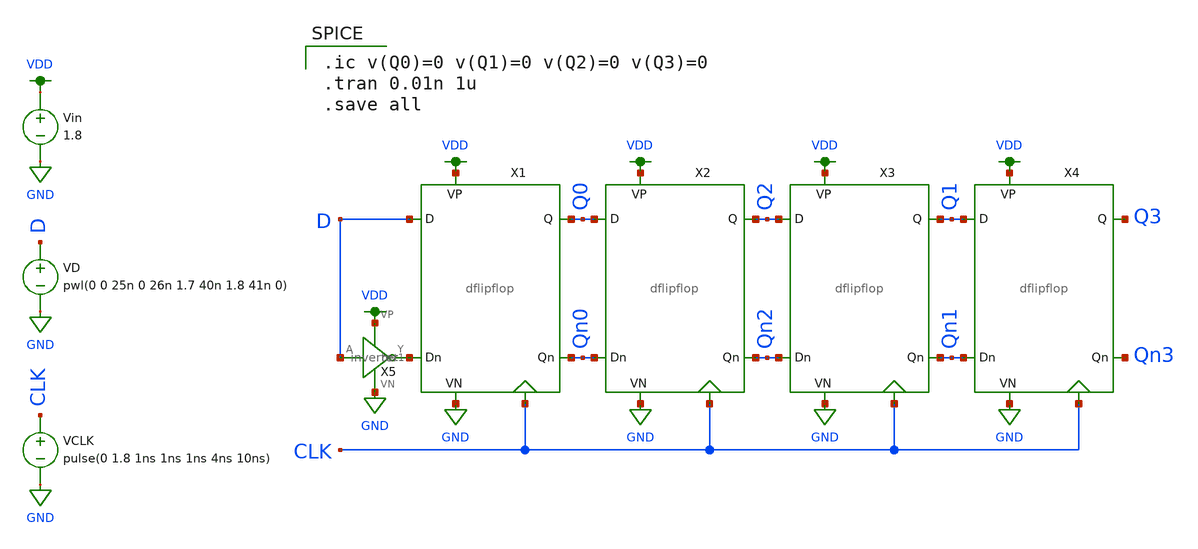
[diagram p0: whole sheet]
** sch_path: miniproject_02/xschem/shiftreg4_tran.sch
**.subckt shiftreg4_tran
X1 D Q0 VDD GND net1 Qn0 CLK dflipflop
X2 Q0 Q2 VDD GND Qn0 Qn2 CLK dflipflop
X3 Q2 Q1 VDD GND Qn2 Qn1 CLK dflipflop
X4 Q1 Q3 VDD GND Qn1 Qn3 CLK dflipflop
X5 D net1 VDD GND inverter
Vin VDD GND 1.8
VD D GND pwl(0 0 25n 0 26n 1.7 40n 1.8 41n 0)
VCLK CLK GND pulse(0 1.8 1ns 1ns 1ns 4ns 10ns)
**** begin user architecture code

.option wnflag=1
.lib ~/skywater/skywater-pdk/libraries/sky130_fd_pr_ngspice/latest/models/sky130.lib.spice tt


.ic v(Q0)=0 v(Q1)=0 v(Q2)=0 v(Q3)=0
.tran 0.01n 1u
.save all

**** end user architecture code
**.ends

* expanding   symbol:  ENGR3426-MADVLSI/miniproject_02/xschem/dflipflop.sym # of pins=7
** sym_path: miniproject_02/xschem/dflipflop.sym
** sch_path: miniproject_02/xschem/dflipflop.sch
.subckt dflipflop D Q VP VN Dn Qn CLK
*.ipin Dn
*.ipin D
*.opin Q
*.opin Qn
*.iopin CLK
*.iopin VP
*.iopin VN
XM1 net1 CLK D VDD sky130_fd_pr__pfet_01v8 L=0.15 W=1 nf=1 ad='int((nf+1)/2) * W/nf * 0.29' as='int((nf+2)/2) * W/nf * 0.29'
+ pd='2*int((nf+1)/2) * (W/nf + 0.29)' ps='2*int((nf+2)/2) * (W/nf + 0.29)' nrd='0.29 / W' nrs='0.29 / W'
+ sa=0 sb=0 sd=0 mult=1 m=1
XM2 net2 CLK Dn VDD sky130_fd_pr__pfet_01v8 L=0.15 W=1 nf=1 ad='int((nf+1)/2) * W/nf * 0.29' as='int((nf+2)/2) * W/nf * 0.29'
+ pd='2*int((nf+1)/2) * (W/nf + 0.29)' ps='2*int((nf+2)/2) * (W/nf + 0.29)' nrd='0.29 / W' nrs='0.29 / W'
+ sa=0 sb=0 sd=0 mult=1 m=1
XM3 Q CLK net1 GND sky130_fd_pr__nfet_01v8 L=0.15 W=1 nf=1 ad='int((nf+1)/2) * W/nf * 0.29' as='int((nf+2)/2) * W/nf * 0.29'
+ pd='2*int((nf+1)/2) * (W/nf + 0.29)' ps='2*int((nf+2)/2) * (W/nf + 0.29)' nrd='0.29 / W' nrs='0.29 / W'
+ sa=0 sb=0 sd=0 mult=1 m=1
XM4 Qn CLK net2 GND sky130_fd_pr__nfet_01v8 L=0.15 W=1 nf=1 ad='int((nf+1)/2) * W/nf * 0.29' as='int((nf+2)/2) * W/nf * 0.29'
+ pd='2*int((nf+1)/2) * (W/nf + 0.29)' ps='2*int((nf+2)/2) * (W/nf + 0.29)' nrd='0.29 / W' nrs='0.29 / W'
+ sa=0 sb=0 sd=0 mult=1 m=1
XM5 net4 CLK VN GND sky130_fd_pr__nfet_01v8 L=0.15 W=4 nf=1 ad='int((nf+1)/2) * W/nf * 0.29' as='int((nf+2)/2) * W/nf * 0.29'
+ pd='2*int((nf+1)/2) * (W/nf + 0.29)' ps='2*int((nf+2)/2) * (W/nf + 0.29)' nrd='0.29 / W' nrs='0.29 / W'
+ sa=0 sb=0 sd=0 mult=1 m=1
XM6 net2 net1 net4 GND sky130_fd_pr__nfet_01v8 L=0.15 W=1 nf=1 ad='int((nf+1)/2) * W/nf * 0.29' as='int((nf+2)/2) * W/nf * 0.29'
+ pd='2*int((nf+1)/2) * (W/nf + 0.29)' ps='2*int((nf+2)/2) * (W/nf + 0.29)' nrd='0.29 / W' nrs='0.29 / W'
+ sa=0 sb=0 sd=0 mult=1 m=1
XM7 net4 net2 net1 GND sky130_fd_pr__nfet_01v8 L=0.15 W=1 nf=1 ad='int((nf+1)/2) * W/nf * 0.29' as='int((nf+2)/2) * W/nf * 0.29'
+ pd='2*int((nf+1)/2) * (W/nf + 0.29)' ps='2*int((nf+2)/2) * (W/nf + 0.29)' nrd='0.29 / W' nrs='0.29 / W'
+ sa=0 sb=0 sd=0 mult=1 m=1
XM8 net2 net1 VP VDD sky130_fd_pr__pfet_01v8 L=0.15 W=1 nf=1 ad='int((nf+1)/2) * W/nf * 0.29' as='int((nf+2)/2) * W/nf * 0.29'
+ pd='2*int((nf+1)/2) * (W/nf + 0.29)' ps='2*int((nf+2)/2) * (W/nf + 0.29)' nrd='0.29 / W' nrs='0.29 / W'
+ sa=0 sb=0 sd=0 mult=1 m=1
XM9 VP net2 net1 VDD sky130_fd_pr__pfet_01v8 L=0.15 W=1 nf=1 ad='int((nf+1)/2) * W/nf * 0.29' as='int((nf+2)/2) * W/nf * 0.29'
+ pd='2*int((nf+1)/2) * (W/nf + 0.29)' ps='2*int((nf+2)/2) * (W/nf + 0.29)' nrd='0.29 / W' nrs='0.29 / W'
+ sa=0 sb=0 sd=0 mult=1 m=1
XM10 net3 CLK VP VDD sky130_fd_pr__pfet_01v8 L=0.15 W=4 nf=1 ad='int((nf+1)/2) * W/nf * 0.29' as='int((nf+2)/2) * W/nf * 0.29'
+ pd='2*int((nf+1)/2) * (W/nf + 0.29)' ps='2*int((nf+2)/2) * (W/nf + 0.29)' nrd='0.29 / W' nrs='0.29 / W'
+ sa=0 sb=0 sd=0 mult=1 m=1
XM11 Qn Q net3 VDD sky130_fd_pr__pfet_01v8 L=0.15 W=1 nf=1 ad='int((nf+1)/2) * W/nf * 0.29' as='int((nf+2)/2) * W/nf * 0.29'
+ pd='2*int((nf+1)/2) * (W/nf + 0.29)' ps='2*int((nf+2)/2) * (W/nf + 0.29)' nrd='0.29 / W' nrs='0.29 / W'
+ sa=0 sb=0 sd=0 mult=1 m=1
XM12 net3 Qn Q VDD sky130_fd_pr__pfet_01v8 L=0.15 W=1 nf=1 ad='int((nf+1)/2) * W/nf * 0.29' as='int((nf+2)/2) * W/nf * 0.29'
+ pd='2*int((nf+1)/2) * (W/nf + 0.29)' ps='2*int((nf+2)/2) * (W/nf + 0.29)' nrd='0.29 / W' nrs='0.29 / W'
+ sa=0 sb=0 sd=0 mult=1 m=1
XM13 Qn Q VN GND sky130_fd_pr__nfet_01v8 L=0.15 W=1 nf=1 ad='int((nf+1)/2) * W/nf * 0.29' as='int((nf+2)/2) * W/nf * 0.29'
+ pd='2*int((nf+1)/2) * (W/nf + 0.29)' ps='2*int((nf+2)/2) * (W/nf + 0.29)' nrd='0.29 / W' nrs='0.29 / W'
+ sa=0 sb=0 sd=0 mult=1 m=1
XM14 VN Qn Q GND sky130_fd_pr__nfet_01v8 L=0.15 W=1 nf=1 ad='int((nf+1)/2) * W/nf * 0.29' as='int((nf+2)/2) * W/nf * 0.29'
+ pd='2*int((nf+1)/2) * (W/nf + 0.29)' ps='2*int((nf+2)/2) * (W/nf + 0.29)' nrd='0.29 / W' nrs='0.29 / W'
+ sa=0 sb=0 sd=0 mult=1 m=1
.ends


* expanding   symbol:  ENGR3426-MADVLSI/miniproject_01/xschem/inverter.sym # of pins=4
** sym_path: miniproject_01/xschem/inverter.sym
** sch_path: miniproject_01/xschem/inverter.sch
.subckt inverter A Y VP VN
*.ipin A
*.iopin VP
*.iopin VN
*.opin Y
XM1 Y A VN VN sky130_fd_pr__nfet_01v8 L=0.15 W=1 nf=1 ad='int((nf+1)/2) * W/nf * 0.29' as='int((nf+2)/2) * W/nf * 0.29'
+ pd='2*int((nf+1)/2) * (W/nf + 0.29)' ps='2*int((nf+2)/2) * (W/nf + 0.29)' nrd='0.29 / W' nrs='0.29 / W'
+ sa=0 sb=0 sd=0 mult=1 m=1
XM2 Y A VP VP sky130_fd_pr__pfet_01v8 L=0.15 W=1 nf=1 ad='int((nf+1)/2) * W/nf * 0.29' as='int((nf+2)/2) * W/nf * 0.29'
+ pd='2*int((nf+1)/2) * (W/nf + 0.29)' ps='2*int((nf+2)/2) * (W/nf + 0.29)' nrd='0.29 / W' nrs='0.29 / W'
+ sa=0 sb=0 sd=0 mult=1 m=1
.ends

.GLOBAL GND
.GLOBAL VDD
.end
